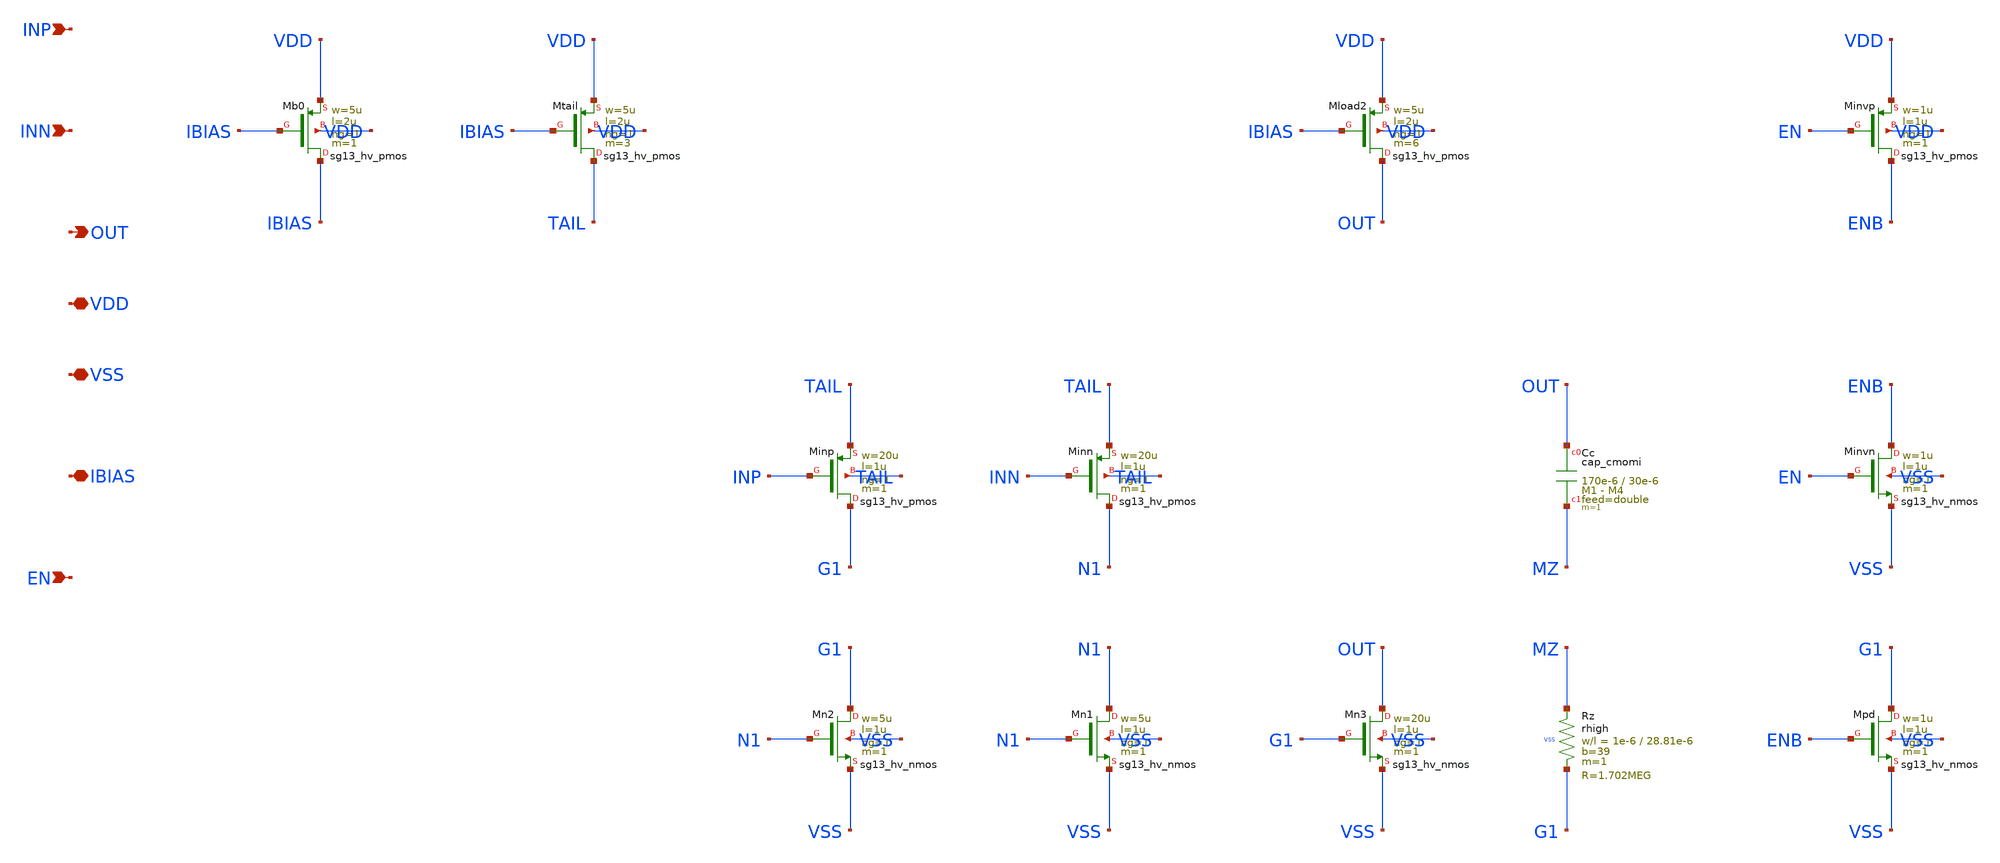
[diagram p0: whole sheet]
** sch_path: design/sg13cmos5l/ldo_erramp_cmos5l.sch
**.subckt ldo_erramp_cmos5l INP INN OUT VDD VSS IBIAS EN
*.ipin INP
*.ipin INN
*.opin OUT
*.iopin VDD
*.iopin VSS
*.iopin IBIAS
*.ipin EN
XMb0 IBIAS IBIAS VDD VDD sg13_hv_pmos w=5u l=2u ng=1 m=1 mm_ok=1
XMtail TAIL IBIAS VDD VDD sg13_hv_pmos w=5u l=2u ng=1 m=3 mm_ok=1
XMload2 OUT IBIAS VDD VDD sg13_hv_pmos w=5u l=2u ng=1 m=6 mm_ok=1
XMinp G1 INP TAIL TAIL sg13_hv_pmos w=20u l=1u ng=1 m=1 mm_ok=1
XMinn N1 INN TAIL TAIL sg13_hv_pmos w=20u l=1u ng=1 m=1 mm_ok=1
XMn2 G1 N1 VSS VSS sg13_hv_nmos w=5u l=1u ng=1 m=1 mm_ok=1
XMn1 N1 N1 VSS VSS sg13_hv_nmos w=5u l=1u ng=1 m=1 mm_ok=1
XMn3 OUT G1 VSS VSS sg13_hv_nmos w=20u l=1u ng=1 m=1 mm_ok=1
XCc OUT MZ cap_cmomi w=170e-6 l=30e-6 mmin=1 mmax=4 feed=double subblock=0 m=1 mm_ok=1
XRz MZ G1 VSS rhigh w=1e-6 l=28.81e-6 m=1 b=39 mm_ok=1
XMinvp ENB EN VDD VDD sg13_hv_pmos w=1u l=1u ng=1 m=1 mm_ok=1
XMinvn ENB EN VSS VSS sg13_hv_nmos w=1u l=1u ng=1 m=1 mm_ok=1
XMpd G1 ENB VSS VSS sg13_hv_nmos w=1u l=1u ng=1 m=1 mm_ok=1
**.ends
.end
